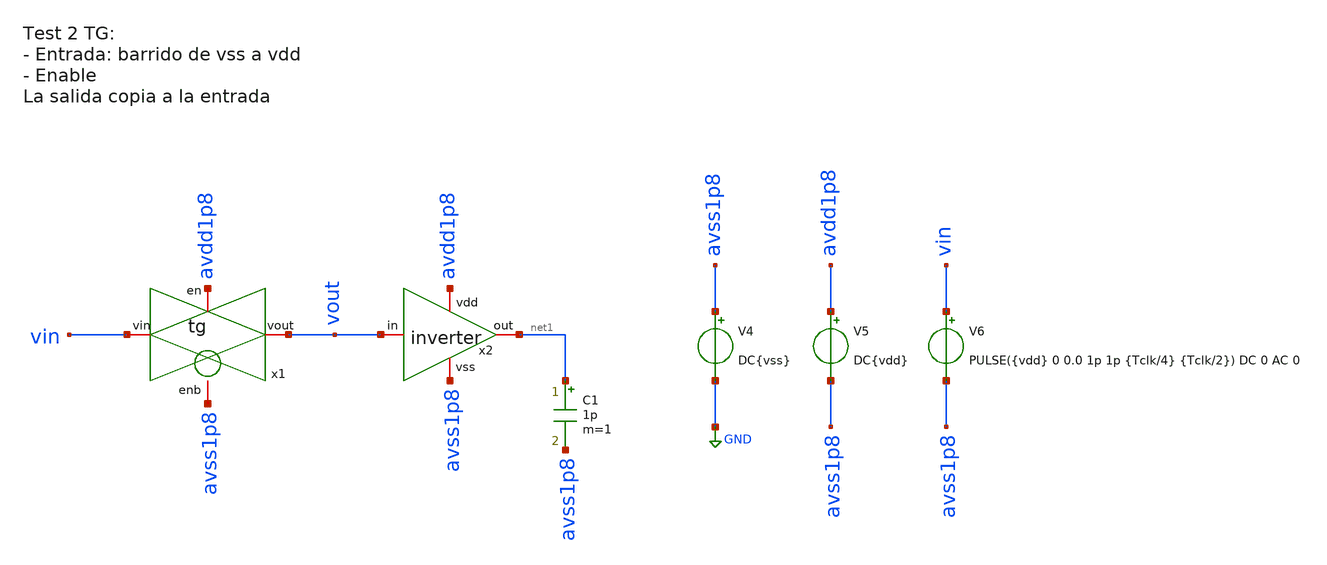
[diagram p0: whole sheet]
** sch_path: designs/sch/tests/test2_tg.sch
**.subckt test2_tg
x2 avdd1p8 net1 vout avss1p8 inverter
V4 avss1p8 GND DC{vss}
V5 avdd1p8 avss1p8 DC{vdd}
V6 vin avss1p8 PULSE({vdd} 0 0.0 1p 1p {Tclk/4} {Tclk/2}) DC 0 AC 0
C1 net1 avss1p8 1p m=1
x1 vin avss1p8 avdd1p8 vout tg
**** begin user architecture code


* Circuit Parameters
.param vdd = 1.8
.param vss = 0.0
.param Tclk = 10n
.options TEMP = 65.0

* Include Models
.lib /foss/pdks/sky130A/libs.tech/ngspice/sky130.lib.spice TT

* OP Parameters & Singals to save
.save all

* Simulations
.control
  tran 0.01u 100n
  setplot tran1
  plot v(vin) v(vout)+2
reset
  dc V6 0 1.8 0.01
  setplot dc
  plot vout ylabel vout xlabel vin
  set filetype = ascii
  write dcsweep.raw
.endc

.end


**** end user architecture code
**.ends

* expanding   symbol:  /foss/designs/sch/inverter.sym # of pins=4
** sym_path: designs/inverter.sym
** sch_path: designs/inverter.sch
.subckt inverter vdd out in vss
*.iopin out
*.iopin vss
*.iopin vdd
*.iopin in
XM2 out in vss vss sky130_fd_pr__nfet_01v8 L=0.15 W=0.75 nf=1 ad='int((nf+1)/2) * W/nf * 0.29' as='int((nf+2)/2) * W/nf * 0.29'
+ pd='2*int((nf+1)/2) * (W/nf + 0.29)' ps='2*int((nf+2)/2) * (W/nf + 0.29)' nrd='0.29 / W' nrs='0.29 / W'
+ sa=0 sb=0 sd=0 mult=1 m=1
XM1 out in vdd vdd sky130_fd_pr__pfet_01v8 L=0.15 W=1.5 nf=1 ad='int((nf+1)/2) * W/nf * 0.29' as='int((nf+2)/2) * W/nf * 0.29'
+ pd='2*int((nf+1)/2) * (W/nf + 0.29)' ps='2*int((nf+2)/2) * (W/nf + 0.29)' nrd='0.29 / W' nrs='0.29 / W'
+ sa=0 sb=0 sd=0 mult=1 m=1
.ends


* expanding   symbol:  /foss/designs/sch/tg.sym # of pins=4
** sym_path: designs/tg.sym
** sch_path: designs/tg.sch
.subckt tg vin enb en vout
*.iopin vin
*.iopin vout
*.iopin enb
*.iopin en
XM1 vin en vout enb sky130_fd_pr__nfet_01v8 L=0.15 W=0.75 nf=1 ad='int((nf+1)/2) * W/nf * 0.29' as='int((nf+2)/2) * W/nf * 0.29'
+ pd='2*int((nf+1)/2) * (W/nf + 0.29)' ps='2*int((nf+2)/2) * (W/nf + 0.29)' nrd='0.29 / W' nrs='0.29 / W'
+ sa=0 sb=0 sd=0 mult=1 m=1
XM2 vout enb vin en sky130_fd_pr__pfet_01v8 L=0.15 W=1.5 nf=1 ad='int((nf+1)/2) * W/nf * 0.29' as='int((nf+2)/2) * W/nf * 0.29'
+ pd='2*int((nf+1)/2) * (W/nf + 0.29)' ps='2*int((nf+2)/2) * (W/nf + 0.29)' nrd='0.29 / W' nrs='0.29 / W'
+ sa=0 sb=0 sd=0 mult=1 m=1
.ends

.GLOBAL GND
.end
